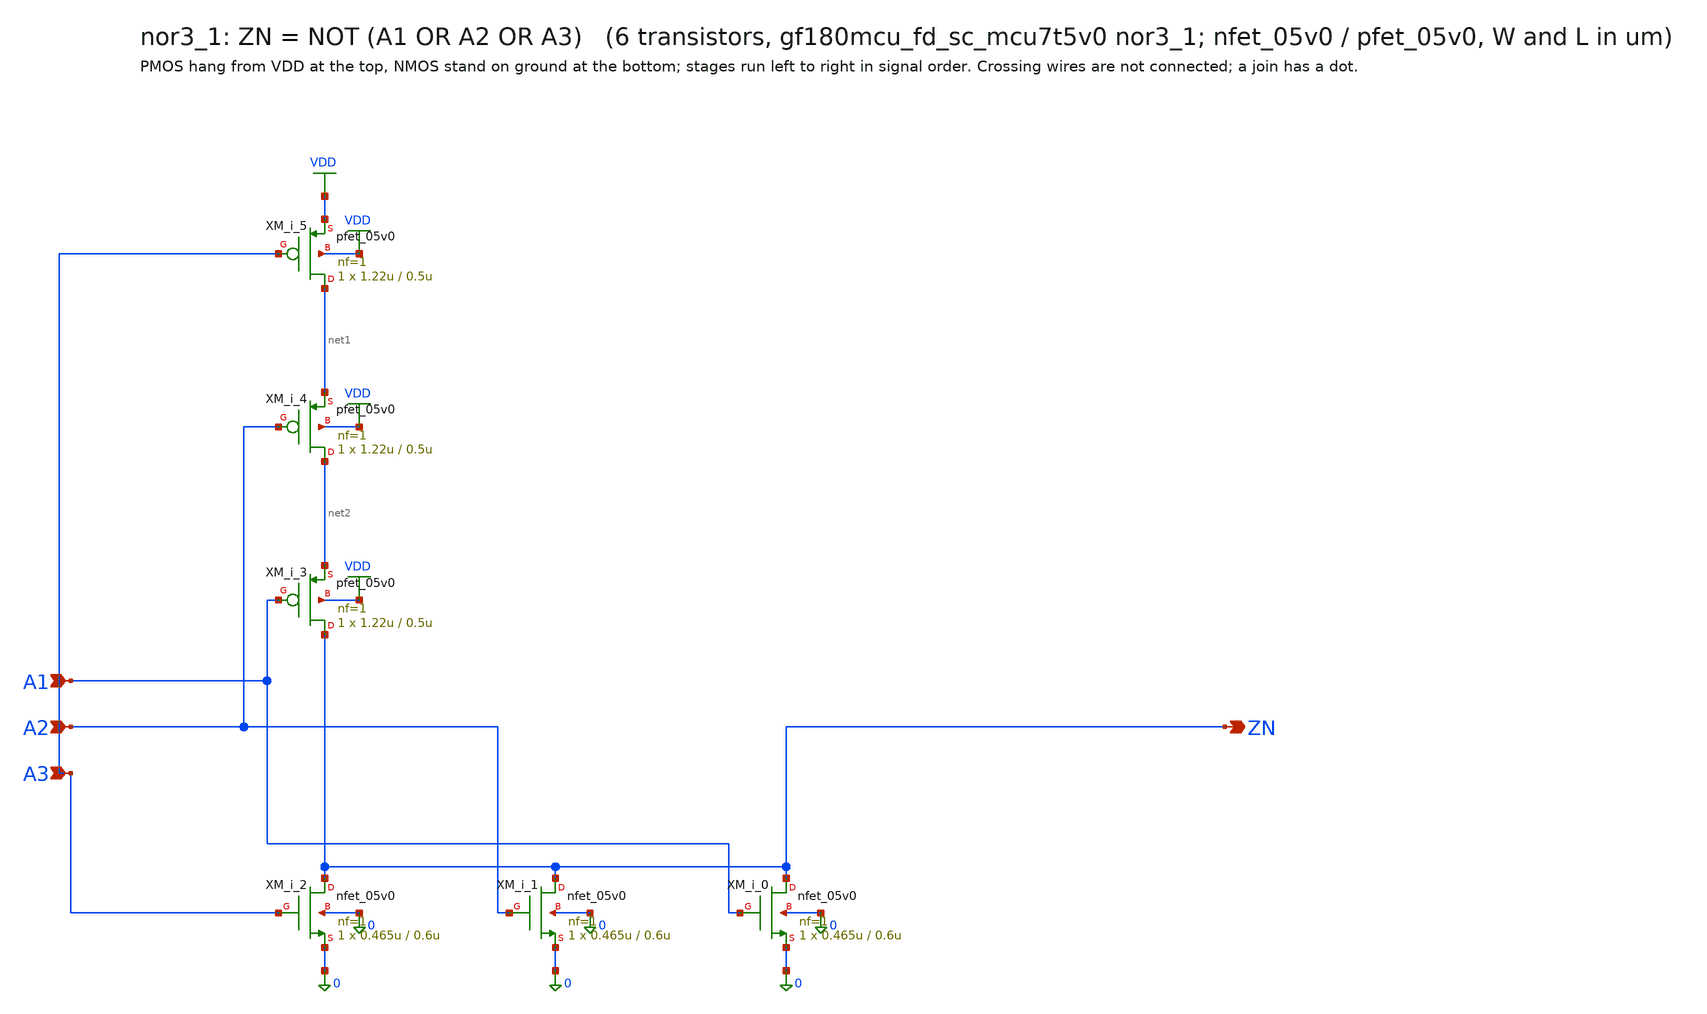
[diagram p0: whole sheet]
** sch_path: xschem/cells_tx/nor3_1.sch
**.subckt nor3_1 A1 A2 A3 ZN
*.ipin A1
*.ipin A2
*.ipin A3
*.opin ZN
XM_i_2 ZN A3 0 0 nfet_05v0 L=0.6u W=0.465u nf=1 ad=2.325e-13 as=2.325e-13 pd=1.93e-06 ps=1.93e-06
+ nrd=0 nrs=0 sa=0 sb=0 sd=0 m=1
XM_i_1 ZN A2 0 0 nfet_05v0 L=0.6u W=0.465u nf=1 ad=2.325e-13 as=2.325e-13 pd=1.93e-06 ps=1.93e-06
+ nrd=0 nrs=0 sa=0 sb=0 sd=0 m=1
XM_i_0 ZN A1 0 0 nfet_05v0 L=0.6u W=0.465u nf=1 ad=2.325e-13 as=2.325e-13 pd=1.93e-06 ps=1.93e-06
+ nrd=0 nrs=0 sa=0 sb=0 sd=0 m=1
XM_i_5 net1 A3 VDD VDD pfet_05v0 L=0.5u W=1.22u nf=1 ad=6.1e-13 as=6.1e-13 pd=3.44e-06 ps=3.44e-06
+ nrd=0 nrs=0 sa=0 sb=0 sd=0 m=1
XM_i_4 net2 A2 net1 VDD pfet_05v0 L=0.5u W=1.22u nf=1 ad=6.1e-13 as=6.1e-13 pd=3.44e-06 ps=3.44e-06
+ nrd=0 nrs=0 sa=0 sb=0 sd=0 m=1
XM_i_3 ZN A1 net2 VDD pfet_05v0 L=0.5u W=1.22u nf=1 ad=6.1e-13 as=6.1e-13 pd=3.44e-06 ps=3.44e-06
+ nrd=0 nrs=0 sa=0 sb=0 sd=0 m=1
**.ends
.GLOBAL VDD
.end
